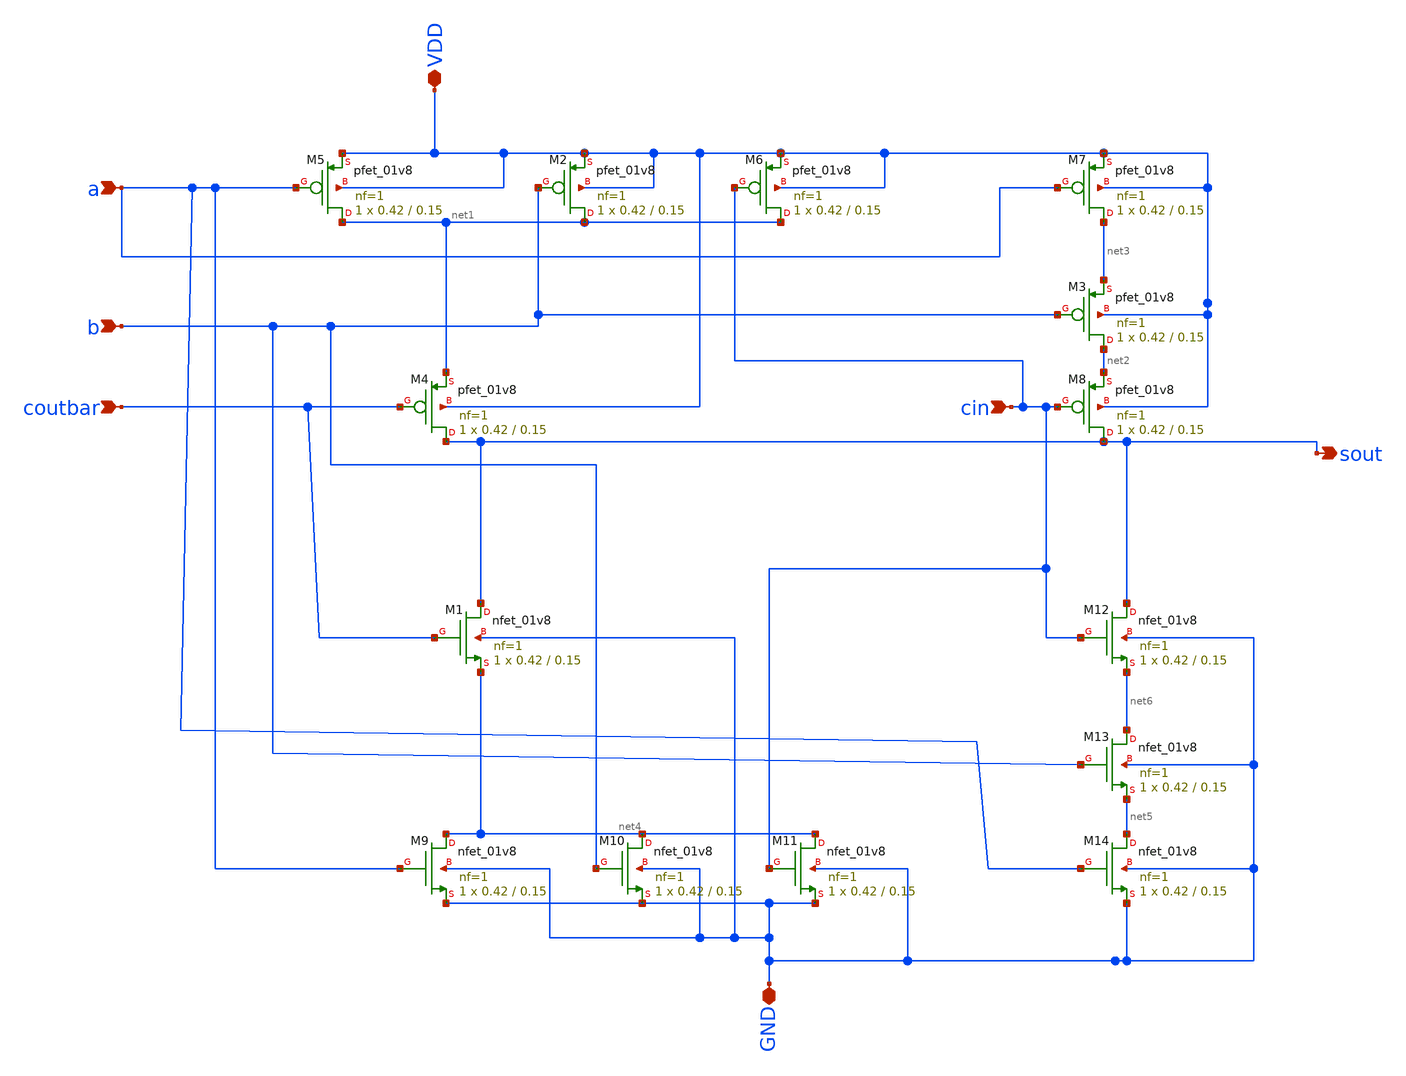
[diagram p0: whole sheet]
** sch_path: assignments/assignment7/sum.sch
**.subckt sum sout a VDD GND b coutbar cin
*.opin sout
*.ipin a
*.iopin VDD
*.iopin GND
*.ipin b
*.ipin coutbar
*.ipin cin
XM1 sout coutbar net4 GND sky130_fd_pr__nfet_01v8 L=0.15 W=0.42 nf=1 ad='int((nf+1)/2) * W/nf * 0.29'
+ as='int((nf+2)/2) * W/nf * 0.29' pd='2*int((nf+1)/2) * (W/nf + 0.29)' ps='2*int((nf+2)/2) * (W/nf + 0.29)'
+ nrd='0.29 / W' nrs='0.29 / W' sa=0 sb=0 sd=0 mult=1 m=1
XM2 net1 b VDD VDD sky130_fd_pr__pfet_01v8 L=0.15 W=0.42 nf=1 ad='int((nf+1)/2) * W/nf * 0.29' as='int((nf+2)/2) * W/nf * 0.29'
+ pd='2*int((nf+1)/2) * (W/nf + 0.29)' ps='2*int((nf+2)/2) * (W/nf + 0.29)' nrd='0.29 / W' nrs='0.29 / W'
+ sa=0 sb=0 sd=0 mult=1 m=1
XM4 sout coutbar net1 VDD sky130_fd_pr__pfet_01v8 L=0.15 W=0.42 nf=1 ad='int((nf+1)/2) * W/nf * 0.29'
+ as='int((nf+2)/2) * W/nf * 0.29' pd='2*int((nf+1)/2) * (W/nf + 0.29)' ps='2*int((nf+2)/2) * (W/nf + 0.29)'
+ nrd='0.29 / W' nrs='0.29 / W' sa=0 sb=0 sd=0 mult=1 m=1
XM5 net1 a VDD VDD sky130_fd_pr__pfet_01v8 L=0.15 W=0.42 nf=1 ad='int((nf+1)/2) * W/nf * 0.29' as='int((nf+2)/2) * W/nf * 0.29'
+ pd='2*int((nf+1)/2) * (W/nf + 0.29)' ps='2*int((nf+2)/2) * (W/nf + 0.29)' nrd='0.29 / W' nrs='0.29 / W'
+ sa=0 sb=0 sd=0 mult=1 m=1
XM6 net1 cin VDD VDD sky130_fd_pr__pfet_01v8 L=0.15 W=0.42 nf=1 ad='int((nf+1)/2) * W/nf * 0.29' as='int((nf+2)/2) * W/nf * 0.29'
+ pd='2*int((nf+1)/2) * (W/nf + 0.29)' ps='2*int((nf+2)/2) * (W/nf + 0.29)' nrd='0.29 / W' nrs='0.29 / W'
+ sa=0 sb=0 sd=0 mult=1 m=1
XM7 net3 a VDD VDD sky130_fd_pr__pfet_01v8 L=0.15 W=0.42 nf=1 ad='int((nf+1)/2) * W/nf * 0.29' as='int((nf+2)/2) * W/nf * 0.29'
+ pd='2*int((nf+1)/2) * (W/nf + 0.29)' ps='2*int((nf+2)/2) * (W/nf + 0.29)' nrd='0.29 / W' nrs='0.29 / W'
+ sa=0 sb=0 sd=0 mult=1 m=1
XM3 net2 b net3 VDD sky130_fd_pr__pfet_01v8 L=0.15 W=0.42 nf=1 ad='int((nf+1)/2) * W/nf * 0.29' as='int((nf+2)/2) * W/nf * 0.29'
+ pd='2*int((nf+1)/2) * (W/nf + 0.29)' ps='2*int((nf+2)/2) * (W/nf + 0.29)' nrd='0.29 / W' nrs='0.29 / W'
+ sa=0 sb=0 sd=0 mult=1 m=1
XM8 sout cin net2 VDD sky130_fd_pr__pfet_01v8 L=0.15 W=0.42 nf=1 ad='int((nf+1)/2) * W/nf * 0.29' as='int((nf+2)/2) * W/nf * 0.29'
+ pd='2*int((nf+1)/2) * (W/nf + 0.29)' ps='2*int((nf+2)/2) * (W/nf + 0.29)' nrd='0.29 / W' nrs='0.29 / W'
+ sa=0 sb=0 sd=0 mult=1 m=1
XM9 net4 a GND GND sky130_fd_pr__nfet_01v8 L=0.15 W=0.42 nf=1 ad='int((nf+1)/2) * W/nf * 0.29' as='int((nf+2)/2) * W/nf * 0.29'
+ pd='2*int((nf+1)/2) * (W/nf + 0.29)' ps='2*int((nf+2)/2) * (W/nf + 0.29)' nrd='0.29 / W' nrs='0.29 / W'
+ sa=0 sb=0 sd=0 mult=1 m=1
XM10 net4 b GND GND sky130_fd_pr__nfet_01v8 L=0.15 W=0.42 nf=1 ad='int((nf+1)/2) * W/nf * 0.29' as='int((nf+2)/2) * W/nf * 0.29'
+ pd='2*int((nf+1)/2) * (W/nf + 0.29)' ps='2*int((nf+2)/2) * (W/nf + 0.29)' nrd='0.29 / W' nrs='0.29 / W'
+ sa=0 sb=0 sd=0 mult=1 m=1
XM11 net4 cin GND GND sky130_fd_pr__nfet_01v8 L=0.15 W=0.42 nf=1 ad='int((nf+1)/2) * W/nf * 0.29' as='int((nf+2)/2) * W/nf * 0.29'
+ pd='2*int((nf+1)/2) * (W/nf + 0.29)' ps='2*int((nf+2)/2) * (W/nf + 0.29)' nrd='0.29 / W' nrs='0.29 / W'
+ sa=0 sb=0 sd=0 mult=1 m=1
XM12 sout cin net6 GND sky130_fd_pr__nfet_01v8 L=0.15 W=0.42 nf=1 ad='int((nf+1)/2) * W/nf * 0.29' as='int((nf+2)/2) * W/nf * 0.29'
+ pd='2*int((nf+1)/2) * (W/nf + 0.29)' ps='2*int((nf+2)/2) * (W/nf + 0.29)' nrd='0.29 / W' nrs='0.29 / W'
+ sa=0 sb=0 sd=0 mult=1 m=1
XM13 net6 b net5 GND sky130_fd_pr__nfet_01v8 L=0.15 W=0.42 nf=1 ad='int((nf+1)/2) * W/nf * 0.29' as='int((nf+2)/2) * W/nf * 0.29'
+ pd='2*int((nf+1)/2) * (W/nf + 0.29)' ps='2*int((nf+2)/2) * (W/nf + 0.29)' nrd='0.29 / W' nrs='0.29 / W'
+ sa=0 sb=0 sd=0 mult=1 m=1
XM14 net5 a GND GND sky130_fd_pr__nfet_01v8 L=0.15 W=0.42 nf=1 ad='int((nf+1)/2) * W/nf * 0.29' as='int((nf+2)/2) * W/nf * 0.29'
+ pd='2*int((nf+1)/2) * (W/nf + 0.29)' ps='2*int((nf+2)/2) * (W/nf + 0.29)' nrd='0.29 / W' nrs='0.29 / W'
+ sa=0 sb=0 sd=0 mult=1 m=1
**.ends
.end
